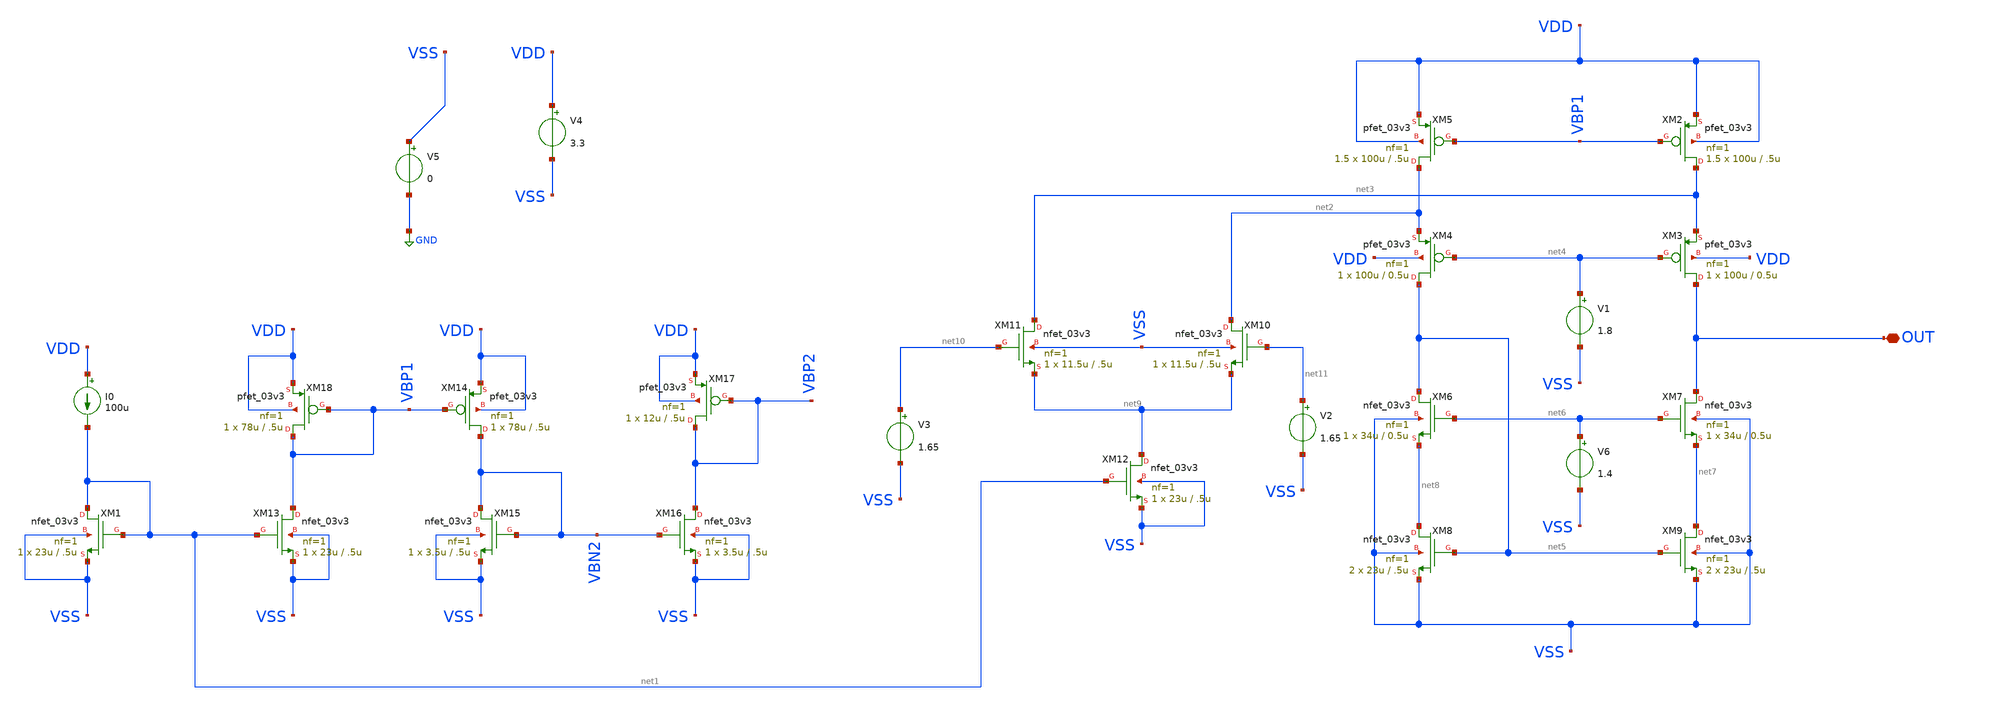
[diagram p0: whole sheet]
** sch_path: designs/libs/tb_amps/tb_ota_folded_cascode/sizing_helper_2.sch
**.subckt sizing_helper_2 OUT
*.iopin OUT
XM1 net1 net1 VSS VSS nfet_03v3 L=.5u W=23u nf=1 ad='int((nf+1)/2) * W/nf * 0.18u' as='int((nf+2)/2) * W/nf * 0.18u'
+ pd='2*int((nf+1)/2) * (W/nf + 0.18u)' ps='2*int((nf+2)/2) * (W/nf + 0.18u)' nrd='0.18u / W' nrs='0.18u / W'
+ sa=0 sb=0 sd=0 m=1
XM2 net3 VBP1 VDD VDD pfet_03v3 L=.5u W=100u nf=1 ad='int((nf+1)/2) * W/nf * 0.18u' as='int((nf+2)/2) * W/nf * 0.18u'
+ pd='2*int((nf+1)/2) * (W/nf + 0.18u)' ps='2*int((nf+2)/2) * (W/nf + 0.18u)' nrd='0.18u / W' nrs='0.18u / W'
+ sa=0 sb=0 sd=0 m=1.5
XM3 OUT net4 net3 VDD pfet_03v3 L=0.5u W=100u nf=1 ad='int((nf+1)/2) * W/nf * 0.18u' as='int((nf+2)/2) * W/nf * 0.18u'
+ pd='2*int((nf+1)/2) * (W/nf + 0.18u)' ps='2*int((nf+2)/2) * (W/nf + 0.18u)' nrd='0.18u / W' nrs='0.18u / W'
+ sa=0 sb=0 sd=0 m=1
XM4 net5 net4 net2 VDD pfet_03v3 L=0.5u W=100u nf=1 ad='int((nf+1)/2) * W/nf * 0.18u' as='int((nf+2)/2) * W/nf * 0.18u'
+ pd='2*int((nf+1)/2) * (W/nf + 0.18u)' ps='2*int((nf+2)/2) * (W/nf + 0.18u)' nrd='0.18u / W' nrs='0.18u / W'
+ sa=0 sb=0 sd=0 m=1
XM5 net2 VBP1 VDD VDD pfet_03v3 L=.5u W=100u nf=1 ad='int((nf+1)/2) * W/nf * 0.18u' as='int((nf+2)/2) * W/nf * 0.18u'
+ pd='2*int((nf+1)/2) * (W/nf + 0.18u)' ps='2*int((nf+2)/2) * (W/nf + 0.18u)' nrd='0.18u / W' nrs='0.18u / W'
+ sa=0 sb=0 sd=0 m=1.5
XM6 net5 net6 net8 VSS nfet_03v3 L=0.5u W=34u nf=1 ad='int((nf+1)/2) * W/nf * 0.18u' as='int((nf+2)/2) * W/nf * 0.18u'
+ pd='2*int((nf+1)/2) * (W/nf + 0.18u)' ps='2*int((nf+2)/2) * (W/nf + 0.18u)' nrd='0.18u / W' nrs='0.18u / W'
+ sa=0 sb=0 sd=0 m=1
XM7 OUT net6 net7 VSS nfet_03v3 L=0.5u W=34u nf=1 ad='int((nf+1)/2) * W/nf * 0.18u' as='int((nf+2)/2) * W/nf * 0.18u'
+ pd='2*int((nf+1)/2) * (W/nf + 0.18u)' ps='2*int((nf+2)/2) * (W/nf + 0.18u)' nrd='0.18u / W' nrs='0.18u / W'
+ sa=0 sb=0 sd=0 m=1
XM8 net8 net5 VSS VSS nfet_03v3 L=.5u W=23u nf=1 ad='int((nf+1)/2) * W/nf * 0.18u' as='int((nf+2)/2) * W/nf * 0.18u'
+ pd='2*int((nf+1)/2) * (W/nf + 0.18u)' ps='2*int((nf+2)/2) * (W/nf + 0.18u)' nrd='0.18u / W' nrs='0.18u / W'
+ sa=0 sb=0 sd=0 m=2
XM9 net7 net5 VSS VSS nfet_03v3 L=.5u W=23u nf=1 ad='int((nf+1)/2) * W/nf * 0.18u' as='int((nf+2)/2) * W/nf * 0.18u'
+ pd='2*int((nf+1)/2) * (W/nf + 0.18u)' ps='2*int((nf+2)/2) * (W/nf + 0.18u)' nrd='0.18u / W' nrs='0.18u / W'
+ sa=0 sb=0 sd=0 m=2
XM10 net2 net11 net9 VSS nfet_03v3 L=.5u W=11.5u nf=1 ad='int((nf+1)/2) * W/nf * 0.18u' as='int((nf+2)/2) * W/nf * 0.18u'
+ pd='2*int((nf+1)/2) * (W/nf + 0.18u)' ps='2*int((nf+2)/2) * (W/nf + 0.18u)' nrd='0.18u / W' nrs='0.18u / W'
+ sa=0 sb=0 sd=0 m=1
XM12 net9 net1 VSS VSS nfet_03v3 L=.5u W=23u nf=1 ad='int((nf+1)/2) * W/nf * 0.18u' as='int((nf+2)/2) * W/nf * 0.18u'
+ pd='2*int((nf+1)/2) * (W/nf + 0.18u)' ps='2*int((nf+2)/2) * (W/nf + 0.18u)' nrd='0.18u / W' nrs='0.18u / W'
+ sa=0 sb=0 sd=0 m=1
XM18 VBP1 VBP1 VDD VDD pfet_03v3 L=.5u W=78u nf=1 ad='int((nf+1)/2) * W/nf * 0.18u' as='int((nf+2)/2) * W/nf * 0.18u'
+ pd='2*int((nf+1)/2) * (W/nf + 0.18u)' ps='2*int((nf+2)/2) * (W/nf + 0.18u)' nrd='0.18u / W' nrs='0.18u / W'
+ sa=0 sb=0 sd=0 m=1
XM11 net3 net10 net9 VSS nfet_03v3 L=.5u W=11.5u nf=1 ad='int((nf+1)/2) * W/nf * 0.18u' as='int((nf+2)/2) * W/nf * 0.18u'
+ pd='2*int((nf+1)/2) * (W/nf + 0.18u)' ps='2*int((nf+2)/2) * (W/nf + 0.18u)' nrd='0.18u / W' nrs='0.18u / W'
+ sa=0 sb=0 sd=0 m=1
XM13 VBP1 net1 VSS VSS nfet_03v3 L=.5u W=23u nf=1 ad='int((nf+1)/2) * W/nf * 0.18u' as='int((nf+2)/2) * W/nf * 0.18u'
+ pd='2*int((nf+1)/2) * (W/nf + 0.18u)' ps='2*int((nf+2)/2) * (W/nf + 0.18u)' nrd='0.18u / W' nrs='0.18u / W'
+ sa=0 sb=0 sd=0 m=1
XM14 VBN2 VBP1 VDD VDD pfet_03v3 L=.5u W=78u nf=1 ad='int((nf+1)/2) * W/nf * 0.18u' as='int((nf+2)/2) * W/nf * 0.18u'
+ pd='2*int((nf+1)/2) * (W/nf + 0.18u)' ps='2*int((nf+2)/2) * (W/nf + 0.18u)' nrd='0.18u / W' nrs='0.18u / W'
+ sa=0 sb=0 sd=0 m=1
XM15 VBN2 VBN2 VSS VSS nfet_03v3 L=.5u W=3.5u nf=1 ad='int((nf+1)/2) * W/nf * 0.18u' as='int((nf+2)/2) * W/nf * 0.18u'
+ pd='2*int((nf+1)/2) * (W/nf + 0.18u)' ps='2*int((nf+2)/2) * (W/nf + 0.18u)' nrd='0.18u / W' nrs='0.18u / W'
+ sa=0 sb=0 sd=0 m=1
XM16 VBP2 VBN2 VSS VSS nfet_03v3 L=.5u W=3.5u nf=1 ad='int((nf+1)/2) * W/nf * 0.18u' as='int((nf+2)/2) * W/nf * 0.18u'
+ pd='2*int((nf+1)/2) * (W/nf + 0.18u)' ps='2*int((nf+2)/2) * (W/nf + 0.18u)' nrd='0.18u / W' nrs='0.18u / W'
+ sa=0 sb=0 sd=0 m=1
XM17 VBP2 VBP2 VDD VDD pfet_03v3 L=.5u W=12u nf=1 ad='int((nf+1)/2) * W/nf * 0.18u' as='int((nf+2)/2) * W/nf * 0.18u'
+ pd='2*int((nf+1)/2) * (W/nf + 0.18u)' ps='2*int((nf+2)/2) * (W/nf + 0.18u)' nrd='0.18u / W' nrs='0.18u / W'
+ sa=0 sb=0 sd=0 m=1
V1 net4 VSS 1.8
V2 net11 VSS 1.65
V3 net10 VSS 1.65
V4 VDD VSS 3.3
I0 VDD net1 100u
V5 VSS GND 0
V6 net6 VSS 1.4
**** begin user architecture code


.control
op
print v(vbp2)
print v(vbn2)
let sat_m1  = abs(@m.xm1.m0[vds]) - abs(@m.xm1.m0[vdsat])
let sat_m2  = abs(@m.xm2.m0[vds]) - abs(@m.xm2.m0[vdsat])
let sat_m3  = abs(@m.xm3.m0[vds]) - abs(@m.xm3.m0[vdsat])
let sat_m4  = abs(@m.xm4.m0[vds]) - abs(@m.xm4.m0[vdsat])
let sat_m5  = abs(@m.xm5.m0[vds]) - abs(@m.xm5.m0[vdsat])
let sat_m6  = abs(@m.xm6.m0[vds]) - abs(@m.xm6.m0[vdsat])
let sat_m7  = abs(@m.xm7.m0[vds]) - abs(@m.xm7.m0[vdsat])
let sat_m8  = abs(@m.xm8.m0[vds]) - abs(@m.xm8.m0[vdsat])
let sat_m9  = abs(@m.xm9.m0[vds]) - abs(@m.xm9.m0[vdsat])
let sat_m10 = abs(@m.xm10.m0[vds]) - abs(@m.xm10.m0[vdsat])
let sat_m11 = abs(@m.xm11.m0[vds]) - abs(@m.xm11.m0[vdsat])
let sat_m12 = abs(@m.xm12.m0[vds]) - abs(@m.xm12.m0[vdsat])
let sat_m13 = abs(@m.xm13.m0[vds]) - abs(@m.xm13.m0[vdsat])
let sat_m18 = abs(@m.xm18.m0[vds]) - abs(@m.xm18.m0[vdsat])
print sat_m1 sat_m2 sat_m3 sat_m4 sat_m5
print sat_m6 sat_m7 sat_m8 sat_m9 sat_m10
print sat_m11 sat_m12 sat_m13 sat_m18
.endc




.include $::180MCU_MODELS/design.ngspice
.lib $::180MCU_MODELS/sm141064.ngspice typical

**** end user architecture code
**.ends
.GLOBAL GND
.end
